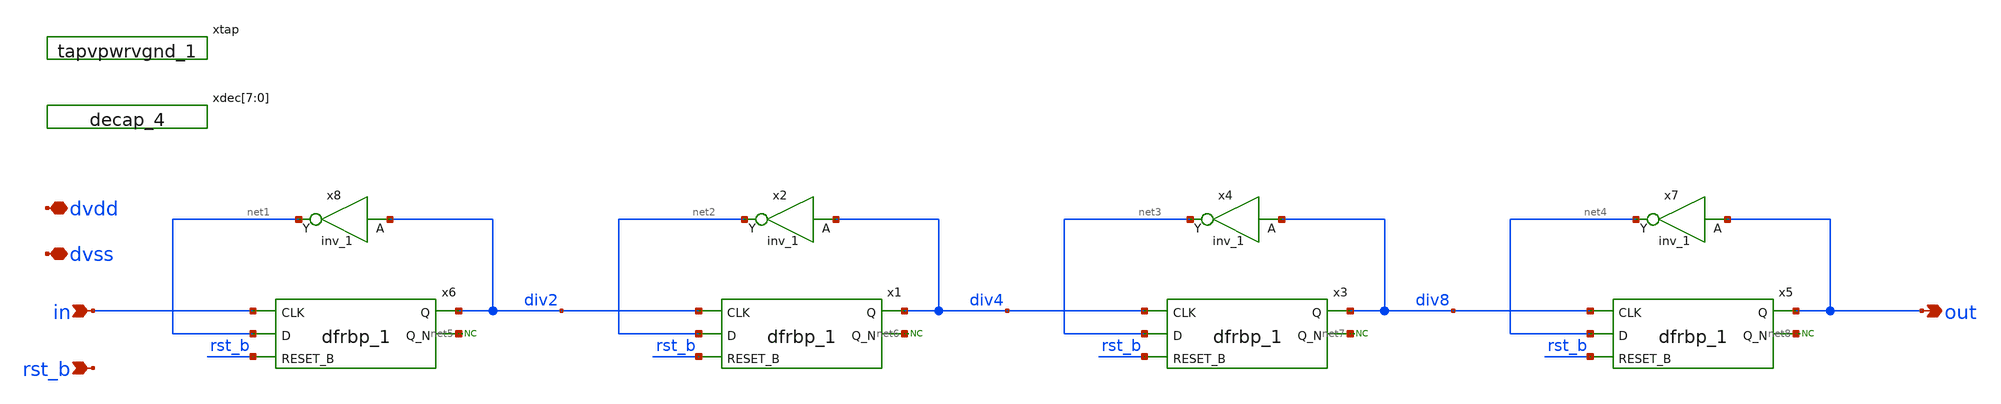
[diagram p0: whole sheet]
** sch_path: xschem/clkdiv/clkdiv.sch
**.subckt clkdiv in rst_b out dvdd dvss
*.ipin in
*.ipin rst_b
*.opin out
*.iopin dvdd
*.iopin dvss
x6 in net1 rst_b dvss dvss dvdd dvdd div2 net5 sky130_fd_sc_hd__dfrbp_1
x8 div2 dvss dvss dvdd dvdd net1 sky130_fd_sc_hd__inv_1
* noconn #net5
x1 div2 net2 rst_b dvss dvss dvdd dvdd div4 net6 sky130_fd_sc_hd__dfrbp_1
x2 div4 dvss dvss dvdd dvdd net2 sky130_fd_sc_hd__inv_1
* noconn #net6
x3 div4 net3 rst_b dvss dvss dvdd dvdd div8 net7 sky130_fd_sc_hd__dfrbp_1
x4 div8 dvss dvss dvdd dvdd net3 sky130_fd_sc_hd__inv_1
* noconn #net7
x5 div8 net4 rst_b dvss dvss dvdd dvdd out net8 sky130_fd_sc_hd__dfrbp_1
x7 out dvss dvss dvdd dvdd net4 sky130_fd_sc_hd__inv_1
* noconn #net8
xdec[7] dvss dvss dvdd dvdd sky130_fd_sc_hd__decap_4
xdec[6] dvss dvss dvdd dvdd sky130_fd_sc_hd__decap_4
xdec[5] dvss dvss dvdd dvdd sky130_fd_sc_hd__decap_4
xdec[4] dvss dvss dvdd dvdd sky130_fd_sc_hd__decap_4
xdec[3] dvss dvss dvdd dvdd sky130_fd_sc_hd__decap_4
xdec[2] dvss dvss dvdd dvdd sky130_fd_sc_hd__decap_4
xdec[1] dvss dvss dvdd dvdd sky130_fd_sc_hd__decap_4
xdec[0] dvss dvss dvdd dvdd sky130_fd_sc_hd__decap_4
xtap dvss dvdd sky130_fd_sc_hd__tapvpwrvgnd_1
**.ends
.end
